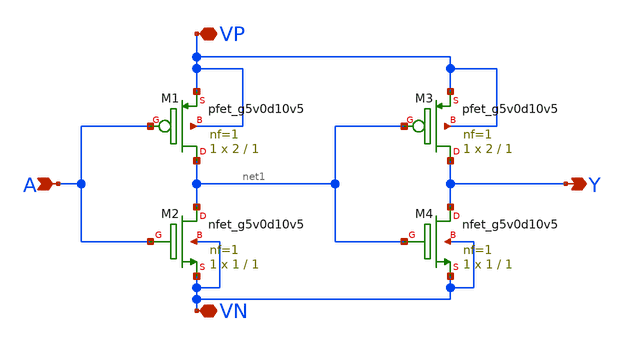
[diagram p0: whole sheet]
** sch_path: ADC/4bit_C2C/MagicAndSpice/shift_5v_to_1v8.sch
**.subckt shift_5v_to_1v8 VN VP A Y
*.iopin VN
*.iopin VP
*.ipin A
*.opin Y
XM1 net1 A VP VP sky130_fd_pr__pfet_g5v0d10v5 L=1 W=2 nf=1 ad='int((nf+1)/2) * W/nf * 0.29' as='int((nf+2)/2) * W/nf * 0.29'
+ pd='2*int((nf+1)/2) * (W/nf + 0.29)' ps='2*int((nf+2)/2) * (W/nf + 0.29)' nrd='0.29 / W' nrs='0.29 / W'
+ sa=0 sb=0 sd=0 mult=1 m=1
XM2 net1 A VN VN sky130_fd_pr__nfet_g5v0d10v5 L=1 W=1 nf=1 ad='int((nf+1)/2) * W/nf * 0.29' as='int((nf+2)/2) * W/nf * 0.29'
+ pd='2*int((nf+1)/2) * (W/nf + 0.29)' ps='2*int((nf+2)/2) * (W/nf + 0.29)' nrd='0.29 / W' nrs='0.29 / W'
+ sa=0 sb=0 sd=0 mult=1 m=1
XM3 Y net1 VP VP sky130_fd_pr__pfet_g5v0d10v5 L=1 W=2 nf=1 ad='int((nf+1)/2) * W/nf * 0.29' as='int((nf+2)/2) * W/nf * 0.29'
+ pd='2*int((nf+1)/2) * (W/nf + 0.29)' ps='2*int((nf+2)/2) * (W/nf + 0.29)' nrd='0.29 / W' nrs='0.29 / W'
+ sa=0 sb=0 sd=0 mult=1 m=1
XM4 Y net1 VN VN sky130_fd_pr__nfet_g5v0d10v5 L=1 W=1 nf=1 ad='int((nf+1)/2) * W/nf * 0.29' as='int((nf+2)/2) * W/nf * 0.29'
+ pd='2*int((nf+1)/2) * (W/nf + 0.29)' ps='2*int((nf+2)/2) * (W/nf + 0.29)' nrd='0.29 / W' nrs='0.29 / W'
+ sa=0 sb=0 sd=0 mult=1 m=1
**.ends
.end
